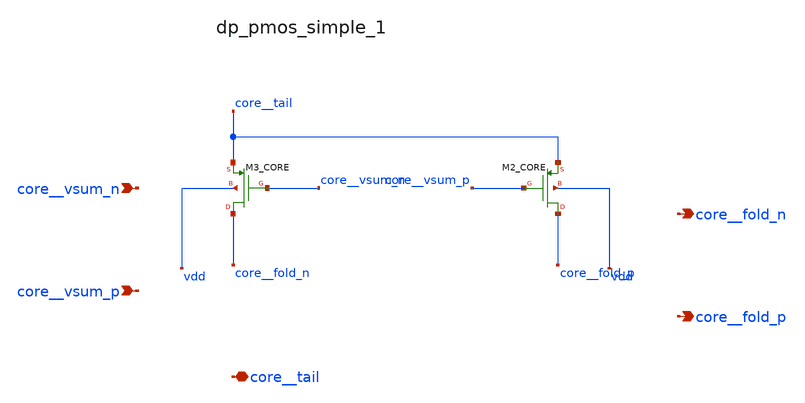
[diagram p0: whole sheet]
** sch_path: analog-db/raw/ia_006_fan_chopper_cmfb/hier/blocks/dp_pmos_simple_1.sch
**.subckt dp_pmos_simple_1 core__vsum_n core__vsum_p core__tail core__fold_n core__fold_p
*.ipin core__vsum_n
*.ipin core__vsum_p
*.iopin core__tail
*.opin core__fold_n
*.opin core__fold_p
XM2_CORE core__fold_p core__vsum_p core__tail vdd sg13_lv_pmos w=x_dut_xm2_core_w l=x_dut_xm2_core_l
+ ng=1 m=x_dut_xm2_core_m
XM3_CORE core__fold_n core__vsum_n core__tail vdd sg13_lv_pmos w=x_dut_xm3_core_w l=x_dut_xm3_core_l
+ ng=1 m=x_dut_xm3_core_m
**.ends
.end
